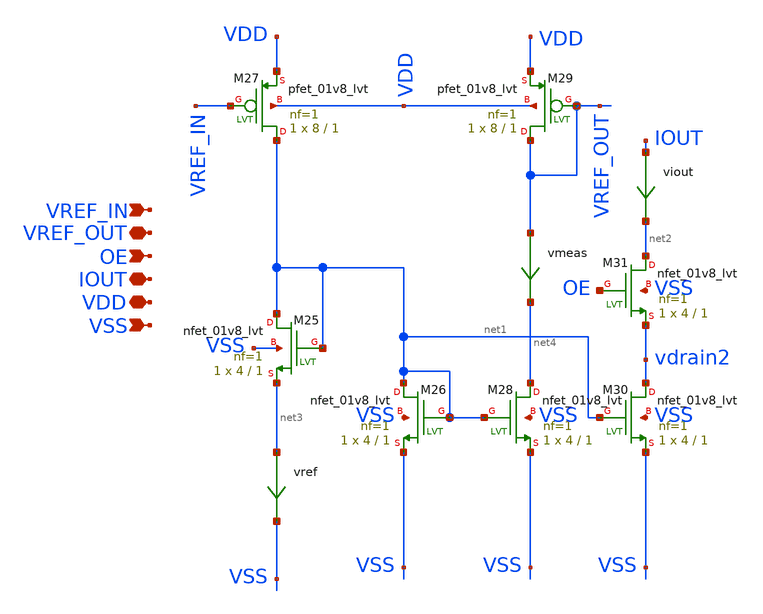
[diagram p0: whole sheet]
** sch_path: xschem/idac1cell.sch
**.subckt idac1cell VSS VREF_OUT VREF_IN VDD IOUT OE
*.ipin VSS
*.iopin VREF_OUT
*.ipin VREF_IN
*.iopin VDD
*.iopin IOUT
*.ipin OE
XM25 net1 net1 net3 VSS sky130_fd_pr__nfet_01v8_lvt L=1 W=4 nf=1 ad='int((nf+1)/2) * W/nf * 0.29' as='int((nf+2)/2) * W/nf * 0.29'
+ pd='2*int((nf+1)/2) * (W/nf + 0.29)' ps='2*int((nf+2)/2) * (W/nf + 0.29)' nrd='0.29 / W' nrs='0.29 / W'
+ sa=0 sb=0 sd=0 mult=1 m=1
XM26 net1 net1 VSS VSS sky130_fd_pr__nfet_01v8_lvt L=1 W=4 nf=1 ad='int((nf+1)/2) * W/nf * 0.29' as='int((nf+2)/2) * W/nf * 0.29'
+ pd='2*int((nf+1)/2) * (W/nf + 0.29)' ps='2*int((nf+2)/2) * (W/nf + 0.29)' nrd='0.29 / W' nrs='0.29 / W'
+ sa=0 sb=0 sd=0 mult=1 m=1
XM27 net1 VREF_IN VDD VDD sky130_fd_pr__pfet_01v8_lvt L=1 W=8 nf=1 ad='int((nf+1)/2) * W/nf * 0.29' as='int((nf+2)/2) * W/nf * 0.29'
+ pd='2*int((nf+1)/2) * (W/nf + 0.29)' ps='2*int((nf+2)/2) * (W/nf + 0.29)' nrd='0.29 / W' nrs='0.29 / W'
+ sa=0 sb=0 sd=0 mult=1 m=1
XM28 net4 net1 VSS VSS sky130_fd_pr__nfet_01v8_lvt L=1 W=4 nf=1 ad='int((nf+1)/2) * W/nf * 0.29' as='int((nf+2)/2) * W/nf * 0.29'
+ pd='2*int((nf+1)/2) * (W/nf + 0.29)' ps='2*int((nf+2)/2) * (W/nf + 0.29)' nrd='0.29 / W' nrs='0.29 / W'
+ sa=0 sb=0 sd=0 mult=1 m=1
XM29 VREF_OUT VREF_OUT VDD VDD sky130_fd_pr__pfet_01v8_lvt L=1 W=8 nf=1 ad='int((nf+1)/2) * W/nf * 0.29'
+ as='int((nf+2)/2) * W/nf * 0.29' pd='2*int((nf+1)/2) * (W/nf + 0.29)' ps='2*int((nf+2)/2) * (W/nf + 0.29)'
+ nrd='0.29 / W' nrs='0.29 / W' sa=0 sb=0 sd=0 mult=1 m=1
XM30 vdrain2 net1 VSS VSS sky130_fd_pr__nfet_01v8_lvt L=1 W=4 nf=1 ad='int((nf+1)/2) * W/nf * 0.29' as='int((nf+2)/2) * W/nf * 0.29'
+ pd='2*int((nf+1)/2) * (W/nf + 0.29)' ps='2*int((nf+2)/2) * (W/nf + 0.29)' nrd='0.29 / W' nrs='0.29 / W'
+ sa=0 sb=0 sd=0 mult=1 m=1
XM31 net2 OE vdrain2 VSS sky130_fd_pr__nfet_01v8_lvt L=1 W=4 nf=1 ad='int((nf+1)/2) * W/nf * 0.29' as='int((nf+2)/2) * W/nf * 0.29'
+ pd='2*int((nf+1)/2) * (W/nf + 0.29)' ps='2*int((nf+2)/2) * (W/nf + 0.29)' nrd='0.29 / W' nrs='0.29 / W'
+ sa=0 sb=0 sd=0 mult=1 m=1
vref net3 VSS 0
.save i(vref)
viout IOUT net2 0
.save i(viout)
vmeas VREF_OUT net4 0
.save i(vmeas)
**.ends
.end
